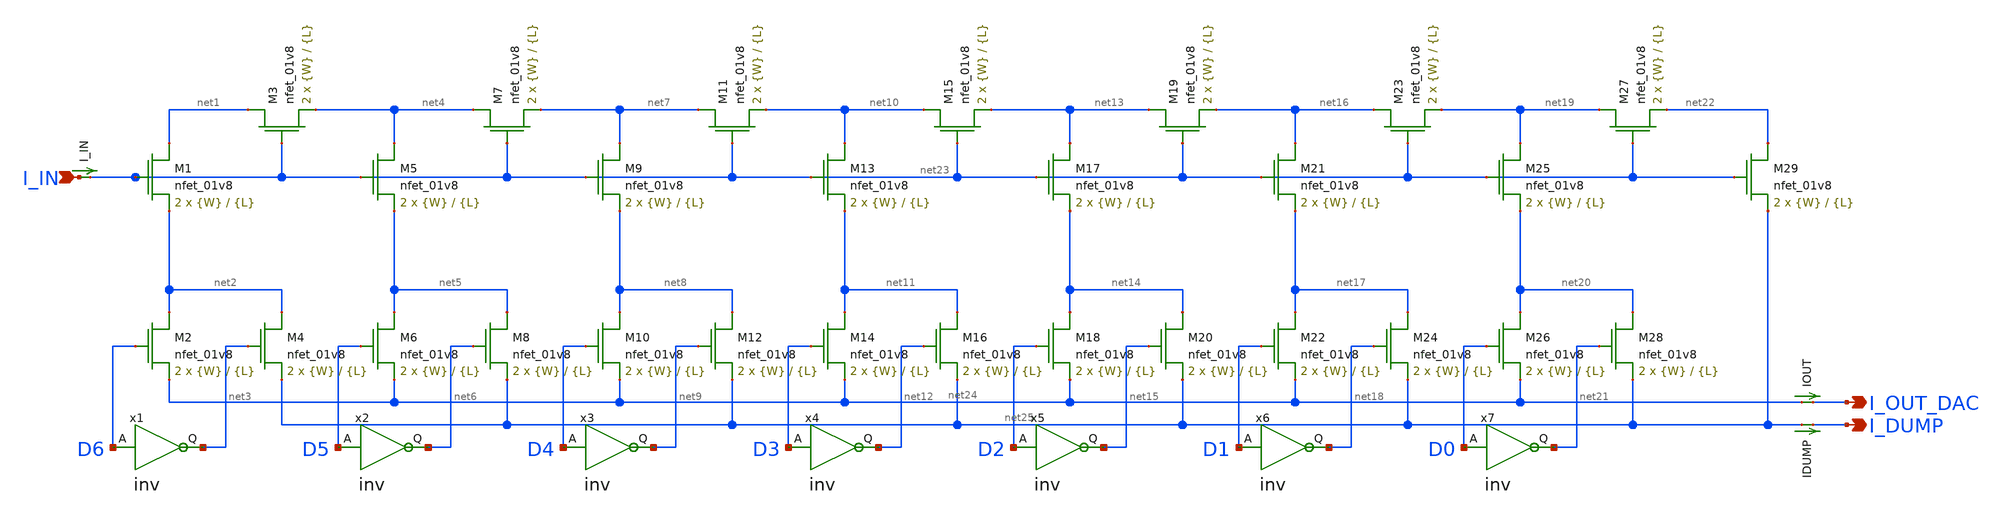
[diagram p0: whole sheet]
** sch_path: schemas/M2M_ladder.sch
**.subckt M2M_ladder I_OUT_DAC I_DUMP I_IN
*.opin I_OUT_DAC
*.opin I_DUMP
*.ipin I_IN
XM1 net1 net23 net2 GND sky130_fd_pr__nfet_01v8 L={L} W={W} nf=1 ad='int((nf+1)/2) * W/nf * 0.29' as='int((nf+2)/2) * W/nf * 0.29'
+ pd='2*int((nf+1)/2) * (W/nf + 0.29)' ps='2*int((nf+2)/2) * (W/nf + 0.29)' nrd='0.29 / W' nrs='0.29 / W'
+ sa=0 sb=0 sd=0 mult=2 m=2
IOUT net24 I_OUT_DAC 0
.save i(iout)
XM2 net2 D6 net24 GND sky130_fd_pr__nfet_01v8 L={L} W={W} nf=1 ad='int((nf+1)/2) * W/nf * 0.29' as='int((nf+2)/2) * W/nf * 0.29'
+ pd='2*int((nf+1)/2) * (W/nf + 0.29)' ps='2*int((nf+2)/2) * (W/nf + 0.29)' nrd='0.29 / W' nrs='0.29 / W'
+ sa=0 sb=0 sd=0 mult=2 m=2
XM3 net1 net23 net4 GND sky130_fd_pr__nfet_01v8 L={L} W={W} nf=1 ad='int((nf+1)/2) * W/nf * 0.29' as='int((nf+2)/2) * W/nf * 0.29'
+ pd='2*int((nf+1)/2) * (W/nf + 0.29)' ps='2*int((nf+2)/2) * (W/nf + 0.29)' nrd='0.29 / W' nrs='0.29 / W'
+ sa=0 sb=0 sd=0 mult=2 m=2
XM4 net2 net3 net25 GND sky130_fd_pr__nfet_01v8 L={L} W={W} nf=1 ad='int((nf+1)/2) * W/nf * 0.29' as='int((nf+2)/2) * W/nf * 0.29'
+ pd='2*int((nf+1)/2) * (W/nf + 0.29)' ps='2*int((nf+2)/2) * (W/nf + 0.29)' nrd='0.29 / W' nrs='0.29 / W'
+ sa=0 sb=0 sd=0 mult=2 m=2
XM5 net4 net23 net5 GND sky130_fd_pr__nfet_01v8 L={L} W={W} nf=1 ad='int((nf+1)/2) * W/nf * 0.29' as='int((nf+2)/2) * W/nf * 0.29'
+ pd='2*int((nf+1)/2) * (W/nf + 0.29)' ps='2*int((nf+2)/2) * (W/nf + 0.29)' nrd='0.29 / W' nrs='0.29 / W'
+ sa=0 sb=0 sd=0 mult=2 m=2
XM6 net5 D5 net24 GND sky130_fd_pr__nfet_01v8 L={L} W={W} nf=1 ad='int((nf+1)/2) * W/nf * 0.29' as='int((nf+2)/2) * W/nf * 0.29'
+ pd='2*int((nf+1)/2) * (W/nf + 0.29)' ps='2*int((nf+2)/2) * (W/nf + 0.29)' nrd='0.29 / W' nrs='0.29 / W'
+ sa=0 sb=0 sd=0 mult=2 m=2
XM7 net4 net23 net7 GND sky130_fd_pr__nfet_01v8 L={L} W={W} nf=1 ad='int((nf+1)/2) * W/nf * 0.29' as='int((nf+2)/2) * W/nf * 0.29'
+ pd='2*int((nf+1)/2) * (W/nf + 0.29)' ps='2*int((nf+2)/2) * (W/nf + 0.29)' nrd='0.29 / W' nrs='0.29 / W'
+ sa=0 sb=0 sd=0 mult=2 m=2
XM8 net5 net6 net25 GND sky130_fd_pr__nfet_01v8 L={L} W={W} nf=1 ad='int((nf+1)/2) * W/nf * 0.29' as='int((nf+2)/2) * W/nf * 0.29'
+ pd='2*int((nf+1)/2) * (W/nf + 0.29)' ps='2*int((nf+2)/2) * (W/nf + 0.29)' nrd='0.29 / W' nrs='0.29 / W'
+ sa=0 sb=0 sd=0 mult=2 m=2
XM9 net7 net23 net8 GND sky130_fd_pr__nfet_01v8 L={L} W={W} nf=1 ad='int((nf+1)/2) * W/nf * 0.29' as='int((nf+2)/2) * W/nf * 0.29'
+ pd='2*int((nf+1)/2) * (W/nf + 0.29)' ps='2*int((nf+2)/2) * (W/nf + 0.29)' nrd='0.29 / W' nrs='0.29 / W'
+ sa=0 sb=0 sd=0 mult=2 m=2
XM10 net8 D4 net24 GND sky130_fd_pr__nfet_01v8 L={L} W={W} nf=1 ad='int((nf+1)/2) * W/nf * 0.29' as='int((nf+2)/2) * W/nf * 0.29'
+ pd='2*int((nf+1)/2) * (W/nf + 0.29)' ps='2*int((nf+2)/2) * (W/nf + 0.29)' nrd='0.29 / W' nrs='0.29 / W'
+ sa=0 sb=0 sd=0 mult=2 m=2
XM11 net7 net23 net10 GND sky130_fd_pr__nfet_01v8 L={L} W={W} nf=1 ad='int((nf+1)/2) * W/nf * 0.29' as='int((nf+2)/2) * W/nf * 0.29'
+ pd='2*int((nf+1)/2) * (W/nf + 0.29)' ps='2*int((nf+2)/2) * (W/nf + 0.29)' nrd='0.29 / W' nrs='0.29 / W'
+ sa=0 sb=0 sd=0 mult=2 m=2
XM12 net8 net9 net25 GND sky130_fd_pr__nfet_01v8 L={L} W={W} nf=1 ad='int((nf+1)/2) * W/nf * 0.29' as='int((nf+2)/2) * W/nf * 0.29'
+ pd='2*int((nf+1)/2) * (W/nf + 0.29)' ps='2*int((nf+2)/2) * (W/nf + 0.29)' nrd='0.29 / W' nrs='0.29 / W'
+ sa=0 sb=0 sd=0 mult=2 m=2
XM13 net10 net23 net11 GND sky130_fd_pr__nfet_01v8 L={L} W={W} nf=1 ad='int((nf+1)/2) * W/nf * 0.29'
+ as='int((nf+2)/2) * W/nf * 0.29' pd='2*int((nf+1)/2) * (W/nf + 0.29)' ps='2*int((nf+2)/2) * (W/nf + 0.29)'
+ nrd='0.29 / W' nrs='0.29 / W' sa=0 sb=0 sd=0 mult=2 m=2
XM14 net11 D3 net24 GND sky130_fd_pr__nfet_01v8 L={L} W={W} nf=1 ad='int((nf+1)/2) * W/nf * 0.29' as='int((nf+2)/2) * W/nf * 0.29'
+ pd='2*int((nf+1)/2) * (W/nf + 0.29)' ps='2*int((nf+2)/2) * (W/nf + 0.29)' nrd='0.29 / W' nrs='0.29 / W'
+ sa=0 sb=0 sd=0 mult=2 m=2
XM15 net10 net23 net13 GND sky130_fd_pr__nfet_01v8 L={L} W={W} nf=1 ad='int((nf+1)/2) * W/nf * 0.29'
+ as='int((nf+2)/2) * W/nf * 0.29' pd='2*int((nf+1)/2) * (W/nf + 0.29)' ps='2*int((nf+2)/2) * (W/nf + 0.29)'
+ nrd='0.29 / W' nrs='0.29 / W' sa=0 sb=0 sd=0 mult=2 m=2
XM16 net11 net12 net25 GND sky130_fd_pr__nfet_01v8 L={L} W={W} nf=1 ad='int((nf+1)/2) * W/nf * 0.29'
+ as='int((nf+2)/2) * W/nf * 0.29' pd='2*int((nf+1)/2) * (W/nf + 0.29)' ps='2*int((nf+2)/2) * (W/nf + 0.29)'
+ nrd='0.29 / W' nrs='0.29 / W' sa=0 sb=0 sd=0 mult=2 m=2
XM17 net13 net23 net14 GND sky130_fd_pr__nfet_01v8 L={L} W={W} nf=1 ad='int((nf+1)/2) * W/nf * 0.29'
+ as='int((nf+2)/2) * W/nf * 0.29' pd='2*int((nf+1)/2) * (W/nf + 0.29)' ps='2*int((nf+2)/2) * (W/nf + 0.29)'
+ nrd='0.29 / W' nrs='0.29 / W' sa=0 sb=0 sd=0 mult=2 m=2
XM18 net14 D2 net24 GND sky130_fd_pr__nfet_01v8 L={L} W={W} nf=1 ad='int((nf+1)/2) * W/nf * 0.29' as='int((nf+2)/2) * W/nf * 0.29'
+ pd='2*int((nf+1)/2) * (W/nf + 0.29)' ps='2*int((nf+2)/2) * (W/nf + 0.29)' nrd='0.29 / W' nrs='0.29 / W'
+ sa=0 sb=0 sd=0 mult=2 m=2
XM19 net13 net23 net16 GND sky130_fd_pr__nfet_01v8 L={L} W={W} nf=1 ad='int((nf+1)/2) * W/nf * 0.29'
+ as='int((nf+2)/2) * W/nf * 0.29' pd='2*int((nf+1)/2) * (W/nf + 0.29)' ps='2*int((nf+2)/2) * (W/nf + 0.29)'
+ nrd='0.29 / W' nrs='0.29 / W' sa=0 sb=0 sd=0 mult=2 m=2
XM20 net14 net15 net25 GND sky130_fd_pr__nfet_01v8 L={L} W={W} nf=1 ad='int((nf+1)/2) * W/nf * 0.29'
+ as='int((nf+2)/2) * W/nf * 0.29' pd='2*int((nf+1)/2) * (W/nf + 0.29)' ps='2*int((nf+2)/2) * (W/nf + 0.29)'
+ nrd='0.29 / W' nrs='0.29 / W' sa=0 sb=0 sd=0 mult=2 m=2
XM21 net16 net23 net17 GND sky130_fd_pr__nfet_01v8 L={L} W={W} nf=1 ad='int((nf+1)/2) * W/nf * 0.29'
+ as='int((nf+2)/2) * W/nf * 0.29' pd='2*int((nf+1)/2) * (W/nf + 0.29)' ps='2*int((nf+2)/2) * (W/nf + 0.29)'
+ nrd='0.29 / W' nrs='0.29 / W' sa=0 sb=0 sd=0 mult=2 m=2
XM22 net17 D1 net24 GND sky130_fd_pr__nfet_01v8 L={L} W={W} nf=1 ad='int((nf+1)/2) * W/nf * 0.29' as='int((nf+2)/2) * W/nf * 0.29'
+ pd='2*int((nf+1)/2) * (W/nf + 0.29)' ps='2*int((nf+2)/2) * (W/nf + 0.29)' nrd='0.29 / W' nrs='0.29 / W'
+ sa=0 sb=0 sd=0 mult=2 m=2
XM23 net16 net23 net19 GND sky130_fd_pr__nfet_01v8 L={L} W={W} nf=1 ad='int((nf+1)/2) * W/nf * 0.29'
+ as='int((nf+2)/2) * W/nf * 0.29' pd='2*int((nf+1)/2) * (W/nf + 0.29)' ps='2*int((nf+2)/2) * (W/nf + 0.29)'
+ nrd='0.29 / W' nrs='0.29 / W' sa=0 sb=0 sd=0 mult=2 m=2
XM24 net17 net18 net25 GND sky130_fd_pr__nfet_01v8 L={L} W={W} nf=1 ad='int((nf+1)/2) * W/nf * 0.29'
+ as='int((nf+2)/2) * W/nf * 0.29' pd='2*int((nf+1)/2) * (W/nf + 0.29)' ps='2*int((nf+2)/2) * (W/nf + 0.29)'
+ nrd='0.29 / W' nrs='0.29 / W' sa=0 sb=0 sd=0 mult=2 m=2
XM25 net19 net23 net20 GND sky130_fd_pr__nfet_01v8 L={L} W={W} nf=1 ad='int((nf+1)/2) * W/nf * 0.29'
+ as='int((nf+2)/2) * W/nf * 0.29' pd='2*int((nf+1)/2) * (W/nf + 0.29)' ps='2*int((nf+2)/2) * (W/nf + 0.29)'
+ nrd='0.29 / W' nrs='0.29 / W' sa=0 sb=0 sd=0 mult=2 m=2
XM26 net20 D0 net24 GND sky130_fd_pr__nfet_01v8 L={L} W={W} nf=1 ad='int((nf+1)/2) * W/nf * 0.29' as='int((nf+2)/2) * W/nf * 0.29'
+ pd='2*int((nf+1)/2) * (W/nf + 0.29)' ps='2*int((nf+2)/2) * (W/nf + 0.29)' nrd='0.29 / W' nrs='0.29 / W'
+ sa=0 sb=0 sd=0 mult=2 m=2
XM27 net19 net23 net22 GND sky130_fd_pr__nfet_01v8 L={L} W={W} nf=1 ad='int((nf+1)/2) * W/nf * 0.29'
+ as='int((nf+2)/2) * W/nf * 0.29' pd='2*int((nf+1)/2) * (W/nf + 0.29)' ps='2*int((nf+2)/2) * (W/nf + 0.29)'
+ nrd='0.29 / W' nrs='0.29 / W' sa=0 sb=0 sd=0 mult=2 m=2
XM28 net20 net21 net25 GND sky130_fd_pr__nfet_01v8 L={L} W={W} nf=1 ad='int((nf+1)/2) * W/nf * 0.29'
+ as='int((nf+2)/2) * W/nf * 0.29' pd='2*int((nf+1)/2) * (W/nf + 0.29)' ps='2*int((nf+2)/2) * (W/nf + 0.29)'
+ nrd='0.29 / W' nrs='0.29 / W' sa=0 sb=0 sd=0 mult=2 m=2
XM29 net22 net23 net25 GND sky130_fd_pr__nfet_01v8 L={L} W={W} nf=1 ad='int((nf+1)/2) * W/nf * 0.29'
+ as='int((nf+2)/2) * W/nf * 0.29' pd='2*int((nf+1)/2) * (W/nf + 0.29)' ps='2*int((nf+2)/2) * (W/nf + 0.29)'
+ nrd='0.29 / W' nrs='0.29 / W' sa=0 sb=0 sd=0 mult=2 m=2
IDUMP net25 I_DUMP 0
.save i(idump)
I_IN I_IN net23 0
.save i(i_in)
x1 net3 D6 inv
x2 net6 D5 inv
x3 net9 D4 inv
x4 net12 D3 inv
x5 net15 D2 inv
x6 net18 D1 inv
x7 net21 D0 inv
**.ends

* expanding   symbol:  /home/mstopyra/Documents/MADVLSI-MP4-DAC/schemas/inv.sym # of pins=2
** sym_path: /home/mstopyra/Documents/MADVLSI-MP4-DAC/schemas/inv.sym
** sch_path: /home/mstopyra/Documents/MADVLSI-MP4-DAC/schemas/inv.sch
.subckt inv Q A
*.ipin A
*.opin Q
XM1 Q A GND GND sky130_fd_pr__nfet_01v8 L=4 W=32 nf=1 ad='int((nf+1)/2) * W/nf * 0.29' as='int((nf+2)/2) * W/nf * 0.29'
+ pd='2*int((nf+1)/2) * (W/nf + 0.29)' ps='2*int((nf+2)/2) * (W/nf + 0.29)' nrd='0.29 / W' nrs='0.29 / W'
+ sa=0 sb=0 sd=0 mult=2 m=2
XM2 Q A VDD VDD sky130_fd_pr__pfet_01v8 L=4 W=32 nf=1 ad='int((nf+1)/2) * W/nf * 0.29' as='int((nf+2)/2) * W/nf * 0.29'
+ pd='2*int((nf+1)/2) * (W/nf + 0.29)' ps='2*int((nf+2)/2) * (W/nf + 0.29)' nrd='0.29 / W' nrs='0.29 / W'
+ sa=0 sb=0 sd=0 mult=1 m=1
.ends

.GLOBAL VDD
.GLOBAL GND
.end
